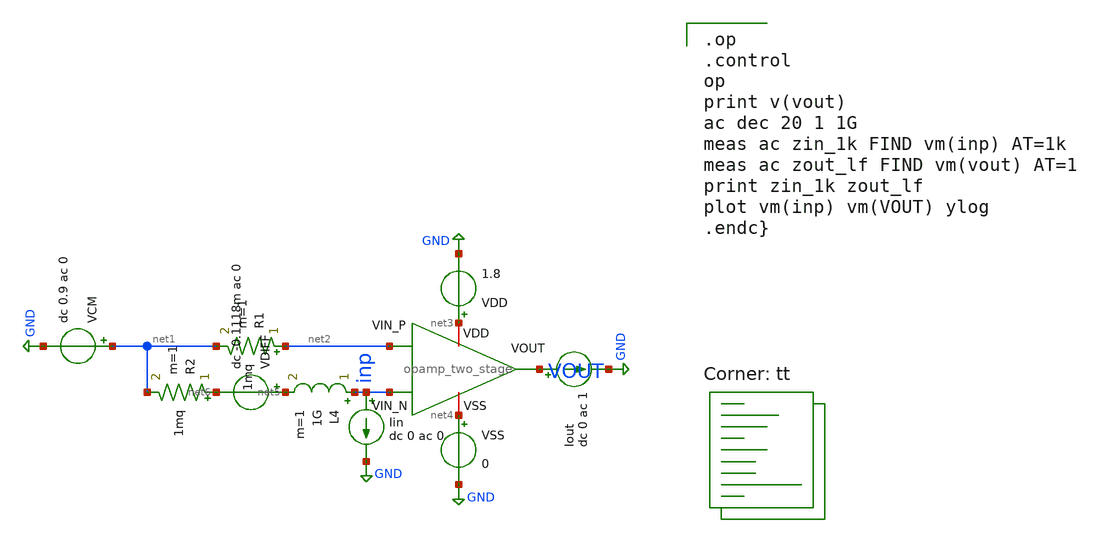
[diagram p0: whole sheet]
** sch_path: analog/bootcamp_opamp/schematics/tb_impedance.sch
**.subckt tb_impedance
x1 net3 VOUT net2 inp net4 opamp_two_stage
VSS net4 GND 0
VDD net3 GND 1.8
VCM net1 GND dc 0.9 ac 0
VDIFF net5 net6 dc -0.1118m ac 0
R1 net2 net1 1mq m=1
R2 net6 net1 1mq m=1
L4 inp net5 1G m=1
Iout VOUT GND dc 0 ac 1
Iin inp GND dc 0 ac 0
**** begin user architecture code

.op
.control
op
print v(vout)
ac dec 20 1 1G
meas ac zin_1k FIND vm(inp) AT=1k
meas ac zout_lf FIND vm(vout) AT=1
print zin_1k zout_lf
plot vm(inp) vm(VOUT) ylog
.endc}

.lib $::SKYWATER_MODELS/sky130.lib.spice tt
**** end user architecture code
**.ends
.GLOBAL GND
.end
